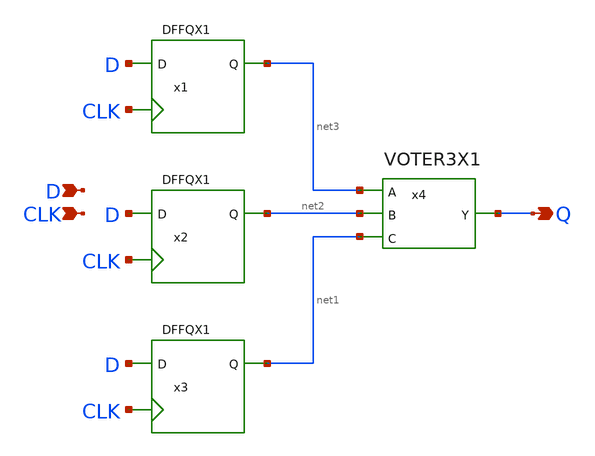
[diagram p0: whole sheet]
** sch_path: archives/lib/xschem/TMRDFFQX1.sch
**.subckt TMRDFFQX1 Q D CLK
*.opin Q
*.ipin D
*.ipin CLK
x1 CLK net3 D VDD VSS DFFQX1
x2 CLK net2 D VDD VSS DFFQX1
x3 CLK net1 D VDD VSS DFFQX1
x4 Q net3 net2 net1 VDD VSS VOTER3X1
**.ends
.end
